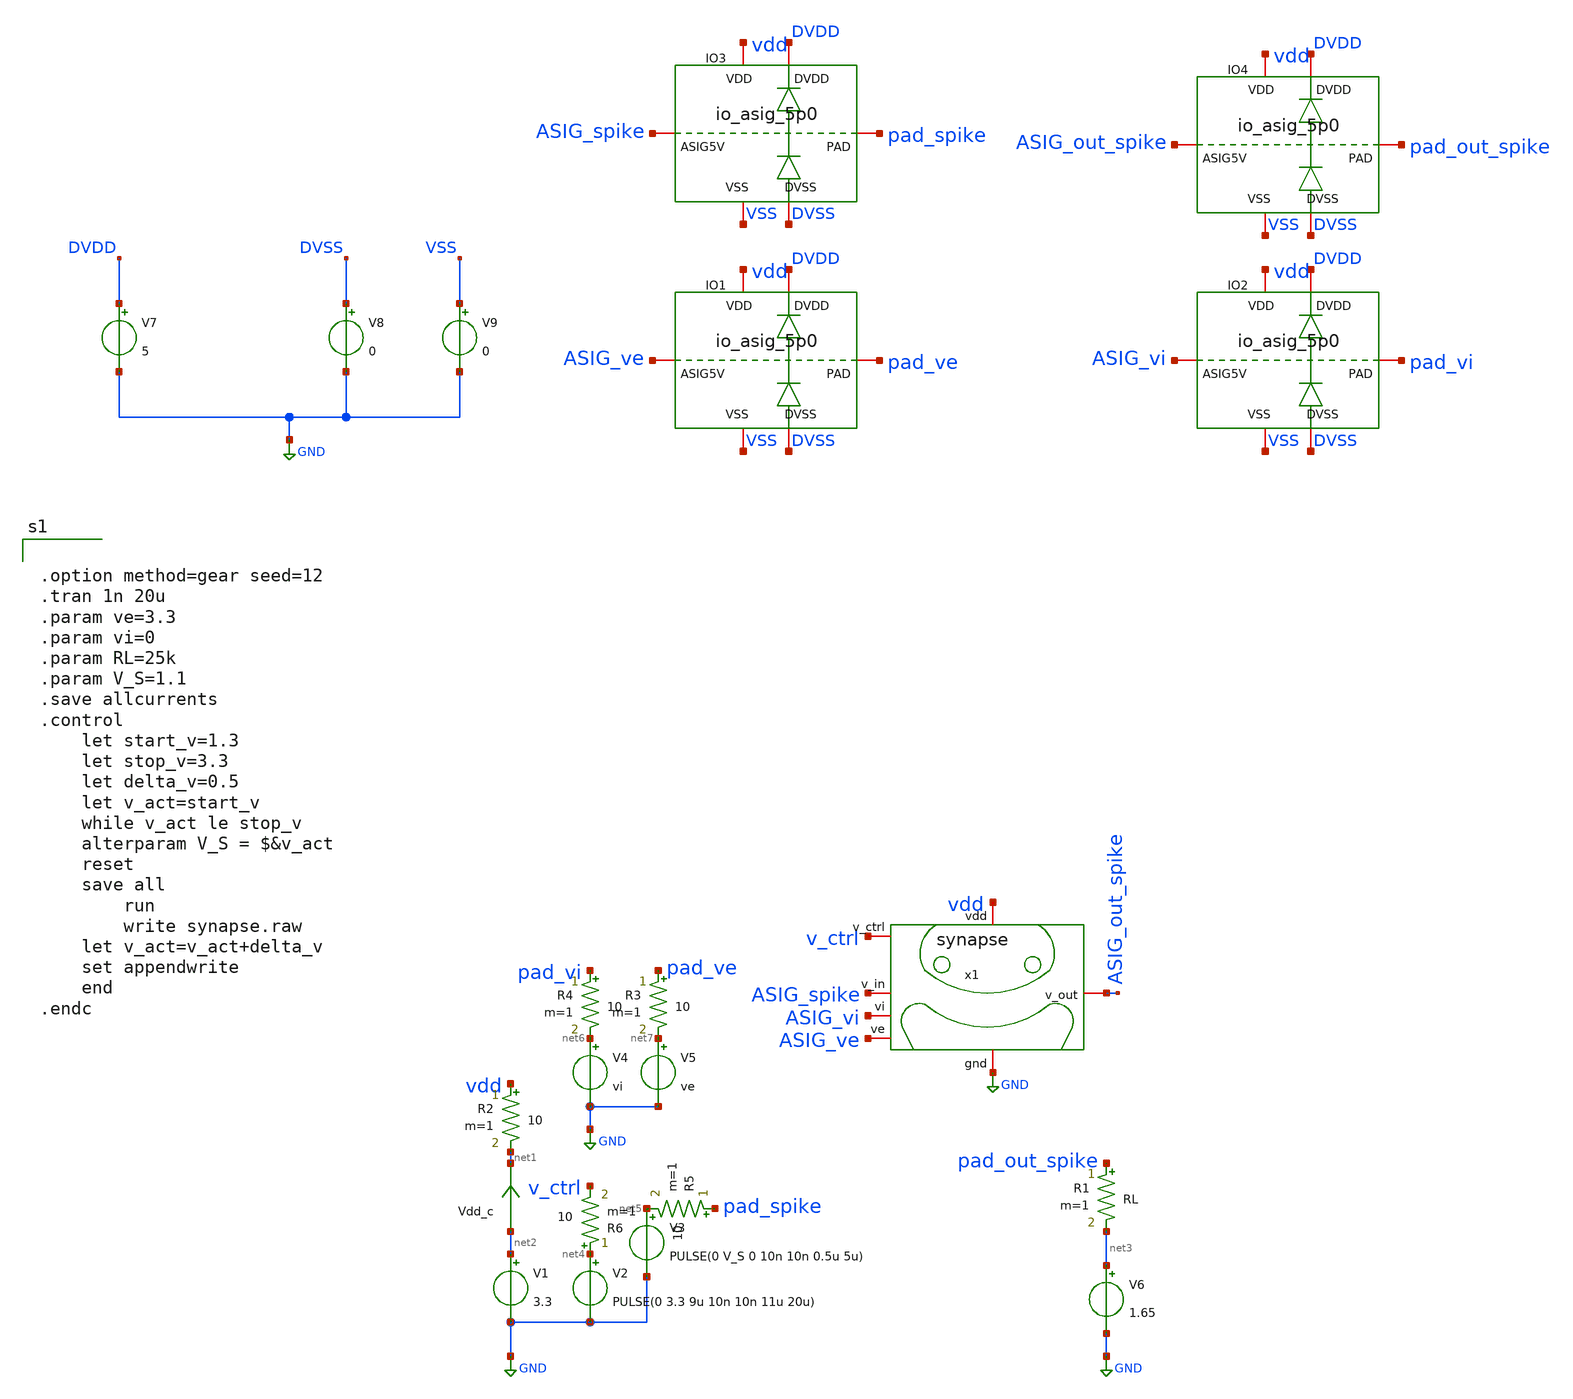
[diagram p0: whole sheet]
** sch_path: designs/pex_PADS/tb_synapse/synapse.sch
**.subckt synapse
V1 net2 GND 3.3
Vdd_c net2 net1 0
.save i(vdd_c)
V2 net4 GND PULSE(0 3.3 9u 10n 10n 11u 20u)
V3 net5 GND PULSE(0 V_S 0 10n 10n 0.5u 5u)
V4 net6 GND vi
V5 net7 GND ve
V6 net3 GND 1.65
R1 pad_out_spike net3 RL m=1
x1 vdd ASIG_spike ASIG_ve v_ctrl ASIG_out_spike ASIG_vi GND synapse
R2 vdd net1 10 m=1
R3 pad_ve net7 10 m=1
R4 pad_vi net6 10 m=1
R5 pad_spike net5 10 m=1
R6 net4 v_ctrl 10 m=1
V7 DVDD GND 5
V8 DVSS GND 0
V9 VSS GND 0
XIO1 DVSS DVDD VSS vdd pad_ve ASIG_ve gf180mcu_fd_io__asig_5p0_extracted
XIO2 DVSS DVDD VSS vdd pad_vi ASIG_vi gf180mcu_fd_io__asig_5p0_extracted
XIO3 DVSS DVDD VSS vdd pad_spike ASIG_spike gf180mcu_fd_io__asig_5p0_extracted
XIO4 DVSS DVDD VSS vdd pad_out_spike ASIG_out_spike gf180mcu_fd_io__asig_5p0_extracted
**** begin user architecture code


.option method=gear seed=12
.tran 1n 20u
.param ve=3.3
.param vi=0
.param RL=25k
.param V_S=1.1
.save allcurrents
.control
    let start_v=1.3
    let stop_v=3.3
    let delta_v=0.5
    let v_act=start_v
    while v_act le stop_v
	alterparam V_S = $&v_act
	reset
	save all
        run
        write synapse.raw
	let v_act=v_act+delta_v
	set appendwrite
    end
.endc



.include $::180MCU_MODELS/design.ngspice
.include /foss/designs/Mosbious_2025_Spikcore/designs/pex/synapse/synapse_pex.spice
.include /foss/designs/Mosbious_2025_Spikcore/miscellaneous/sscs-chipathon/resources/Integration/Chipathon2025_pads/xschem/gf180mcu_fd_io__asig_5p0_extracted.spice
.lib $::180MCU_MODELS/sm141064.ngspice typical
.lib $::180MCU_MODELS/sm141064.ngspice cap_mim
.lib $::180MCU_MODELS/sm141064.ngspice res_typical
.lib $::180MCU_MODELS/sm141064.ngspice moscap_typical
.lib $::180MCU_MODELS/sm141064.ngspice mimcap_typical

**** end user architecture code
**.ends
.GLOBAL GND
.end
